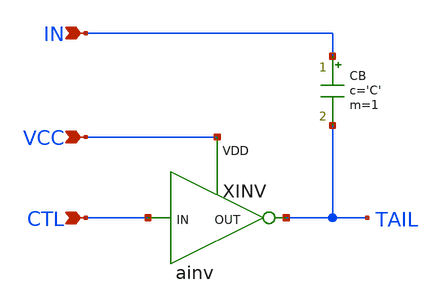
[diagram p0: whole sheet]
** sch_path: xschem_libraries_oa/ngspice_verilog_cosim/ccap/schematic/ccap.sch
**.subckt ccap IN VCC CTL
*.ipin IN
*.ipin VCC
*.ipin CTL
XINV CTL TAIL VCC ainv
CB IN TAIL c='C' m=1
**.ends

* expanding   symbol:  ngspice_verilog_cosim/ainv.sym # of pins=3
** sym_path: ngspice_verilog_cosim/ainv.sym
** sch_path: ngspice_verilog_cosim/ainv.sch
.subckt ainv IN OUT VDD
*.ipin IN
*.opin OUT
*.ipin VDD
MN OUT IN 0 0 N1
MP OUT IN VDD VDD P1
.ends

**** begin user architecture code
.model n1 nmos   level=2 vto=0.5 kp=24e-6 gamma=0.15 phi=0.65 lambda=0.015 xj=0.5e-6

.model p1 pmos   level=2 vto=-0.5 kp=8.5e-6 gamma=0.4 phi=0.65 lambda=0.05 xj=0.5e-6

**** end user architecture code
.end
